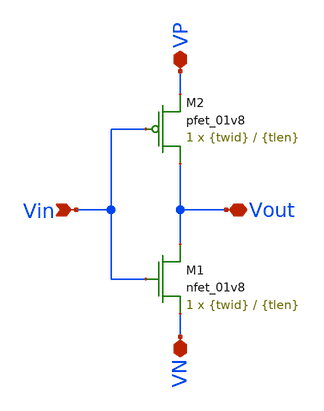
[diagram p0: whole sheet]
** sch_path: prelim-files/inv.sch
**.subckt inv VP VN Vin Vout
*.iopin VP
*.iopin VN
*.ipin Vin
*.iopin Vout
XM1 Vout Vin VN GND sky130_fd_pr__nfet_01v8 L={tlen} W={twid} nf=1 ad='int((nf+1)/2) * W/nf * 0.29' as='int((nf+2)/2) * W/nf * 0.29'
+ pd='2*int((nf+1)/2) * (W/nf + 0.29)' ps='2*int((nf+2)/2) * (W/nf + 0.29)' nrd='0.29 / W' nrs='0.29 / W'
+ sa=0 sb=0 sd=0 mult=1 m=1
XM2 Vout Vin VP VDD sky130_fd_pr__pfet_01v8 L={tlen} W={twid} nf=1 ad='int((nf+1)/2) * W/nf * 0.29' as='int((nf+2)/2) * W/nf * 0.29'
+ pd='2*int((nf+1)/2) * (W/nf + 0.29)' ps='2*int((nf+2)/2) * (W/nf + 0.29)' nrd='0.29 / W' nrs='0.29 / W'
+ sa=0 sb=0 sd=0 mult=1 m=1
**.ends
.end
